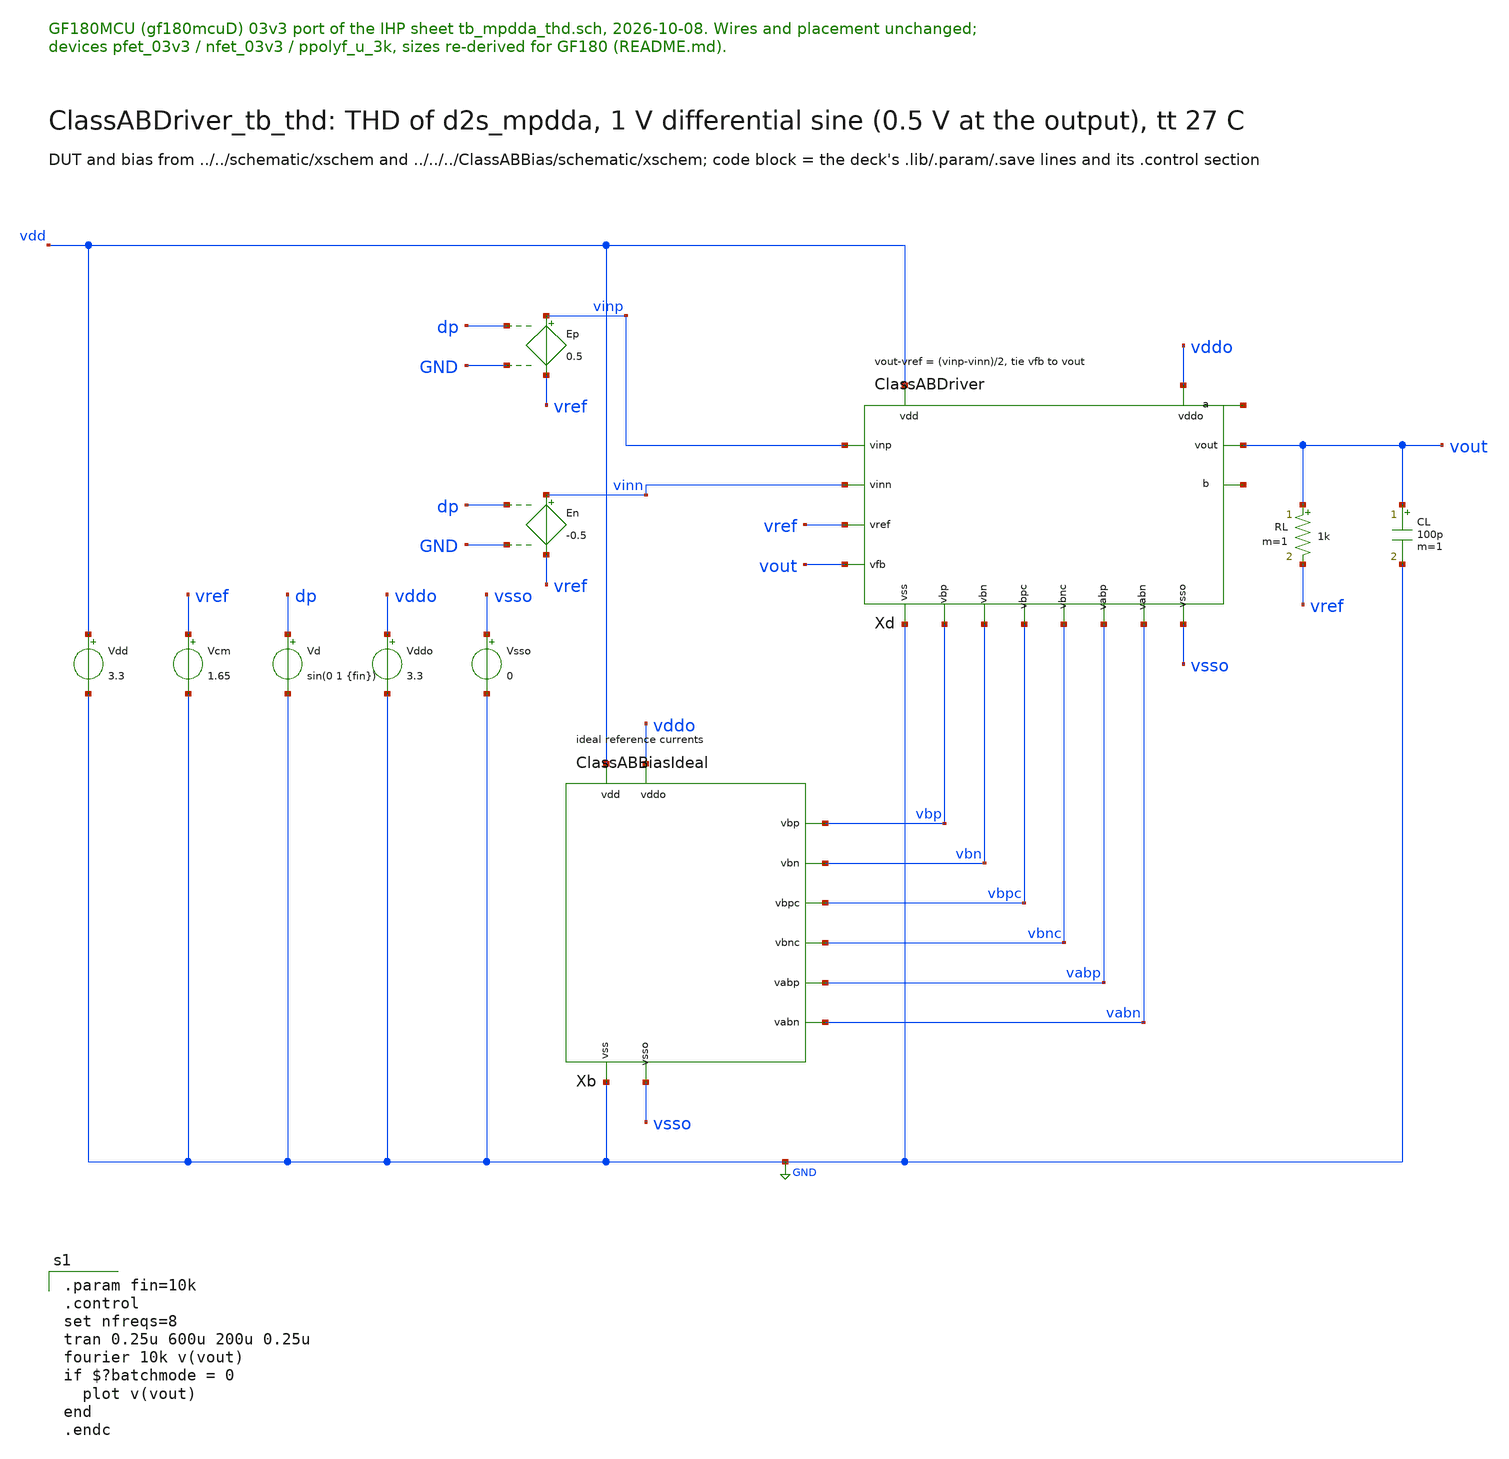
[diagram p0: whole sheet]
** sch_path: macros/ClassABDriver/testbenches/xschem/ClassABDriver_tb_thd.sch
**.subckt ClassABDriver_tb_thd
Vdd vdd GND 3.3
Vcm vref GND 1.65
Xb vdd GND vddo vsso vbp vbn vbpc vbnc vabp vabn ClassABBiasIdeal
Xd vdd GND vddo vsso vinp vinn vref vout vout vbp vbn vbpc vbnc vabp vabn net1 net2 ClassABDriver
Vd dp GND sin(0 1 {fin})
Ep vinp vref dp GND 0.5
En vinn vref dp GND -0.5
RL vout vref 1k m=1
CL vout GND 100p m=1
Vddo vddo GND 3.3
Vsso vsso GND 0
**** begin user architecture code

.param fin=10k
.control
set nfreqs=8
tran 0.25u 600u 200u 0.25u
fourier 10k v(vout)
if $?batchmode = 0
  plot v(vout)
end
.endc


.include $::180MCU_MODELS/design.ngspice
.lib $::180MCU_MODELS/sm141064.ngspice typical
.lib $::180MCU_MODELS/sm141064.ngspice res_typical
.lib $::180MCU_MODELS/sm141064.ngspice moscap_typical

**** end user architecture code
**.ends
.GLOBAL GND
.end
